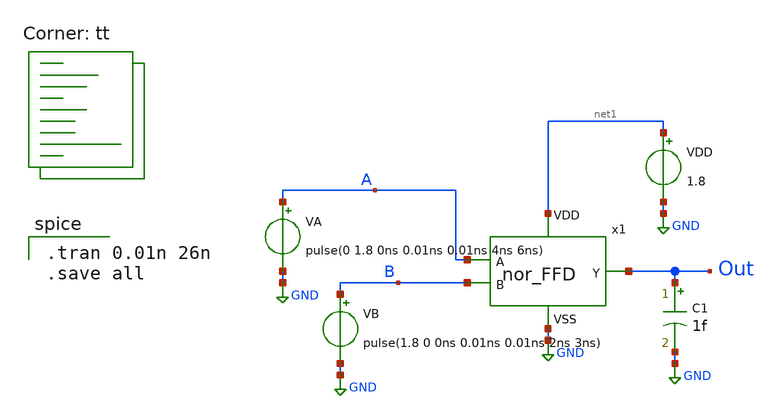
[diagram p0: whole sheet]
** sch_path: nor_FFD_tb.sch
**.subckt nor_FFD_tb
x1 net1 A B Out GND nor_FFD
VA A GND pulse(0 1.8 0ns 0.01ns 0.01ns 4ns 6ns)
VB B GND pulse(1.8 0 0ns 0.01ns 0.01ns 2ns 3ns)
VDD net1 GND 1.8
C1 Out GND 1f m=1
**** begin user architecture code
.lib $::SKYWATER_MODELS/sky130.lib.spice tt

.tran 0.01n 26n
.save all

**** end user architecture code
**.ends

* expanding   symbol:  project/nor_FFD.sym # of pins=5
** sym_path: nor_FFD.sym
** sch_path: nor_FFD.sch
.subckt nor_FFD VDD A B Y VSS
*.ipin VDD
*.ipin A
*.ipin B
*.ipin VSS
*.opin Y
XM1 Y A VSS VSS sky130_fd_pr__nfet_01v8 L=0.15 W=0.5 nf=1 ad='int((nf+1)/2) * W/nf * 0.29' as='int((nf+2)/2) * W/nf * 0.29'
+ pd='2*int((nf+1)/2) * (W/nf + 0.29)' ps='2*int((nf+2)/2) * (W/nf + 0.29)' nrd='0.29 / W' nrs='0.29 / W'
+ sa=0 sb=0 sd=0 mult=1 m=1
XM2 Y B VSS VSS sky130_fd_pr__nfet_01v8 L=0.15 W=0.5 nf=1 ad='int((nf+1)/2) * W/nf * 0.29' as='int((nf+2)/2) * W/nf * 0.29'
+ pd='2*int((nf+1)/2) * (W/nf + 0.29)' ps='2*int((nf+2)/2) * (W/nf + 0.29)' nrd='0.29 / W' nrs='0.29 / W'
+ sa=0 sb=0 sd=0 mult=1 m=1
XM3 net1 A VDD VDD sky130_fd_pr__pfet_01v8 L=0.15 W=2.5 nf=1 ad='int((nf+1)/2) * W/nf * 0.29' as='int((nf+2)/2) * W/nf * 0.29'
+ pd='2*int((nf+1)/2) * (W/nf + 0.29)' ps='2*int((nf+2)/2) * (W/nf + 0.29)' nrd='0.29 / W' nrs='0.29 / W'
+ sa=0 sb=0 sd=0 mult=1 m=1
XM4 Y B net1 VDD sky130_fd_pr__pfet_01v8 L=0.15 W=2.5 nf=1 ad='int((nf+1)/2) * W/nf * 0.29' as='int((nf+2)/2) * W/nf * 0.29'
+ pd='2*int((nf+1)/2) * (W/nf + 0.29)' ps='2*int((nf+2)/2) * (W/nf + 0.29)' nrd='0.29 / W' nrs='0.29 / W'
+ sa=0 sb=0 sd=0 mult=1 m=1
.ends

.GLOBAL GND
.end
